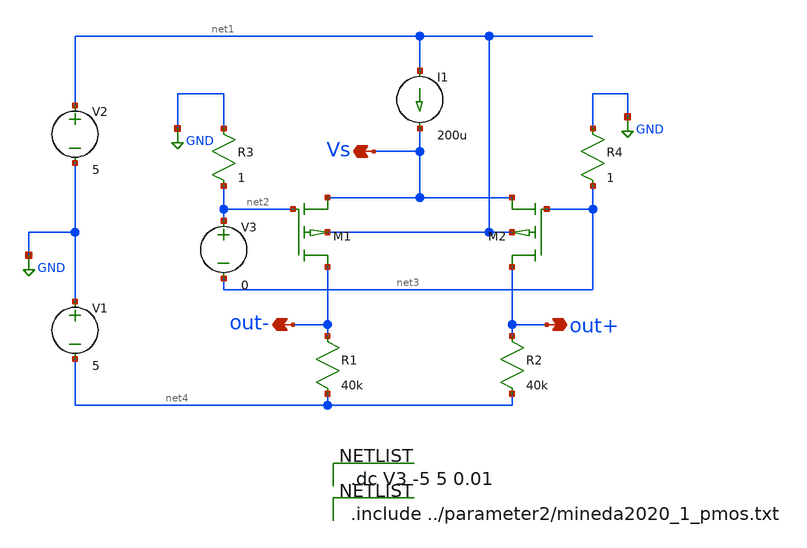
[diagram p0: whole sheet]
** sch_path: diffamp_test10um.sch
**.subckt diffamp_test10um out- out+ Vs
*.opin out-
*.opin out+
*.opin Vs
V1 GND net4 5
M2 out+ net3 Vs net1 YSS_PMOS w=100u l=10u as=0 ps=0 ad=0 pd=0 m=1
V3 net2 net3 0
M1 out- net2 Vs net1 YSS_PMOS w=100u l=10u as=0 ps=0 ad=0 pd=0 m=1
V2 net1 GND 5
R1 out- net4 40k m=1
R2 out+ net4 40k m=1
I1 net1 Vs 200u
R3 GND net2 1 m=1
R4 GND net3 1 m=1
**** begin user architecture code

.dc V3 -5 5 0.01


.include ../parameter2/mineda2020_1_pmos.txt

**** end user architecture code
**.ends
.GLOBAL GND
.end
